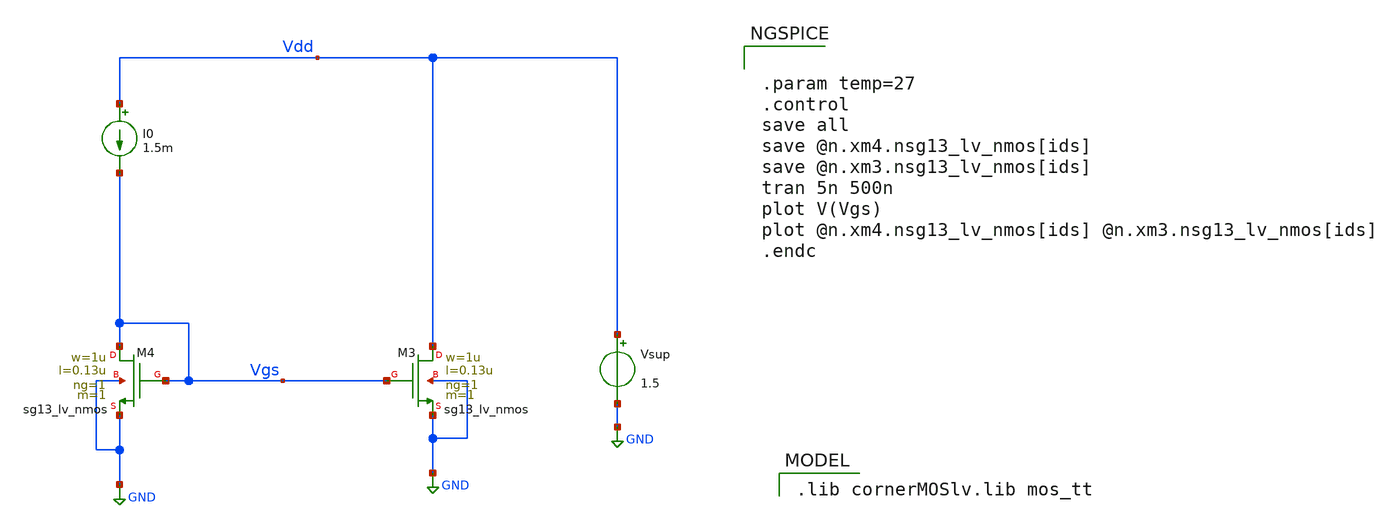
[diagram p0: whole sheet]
** sch_path: xschem/current_mirror.sch
**.subckt current_mirror
XM3 Vdd Vgs GND GND sg13_lv_nmos w=1u l=0.13u ng=1 m=1 mm_ok=1
XM4 Vgs Vgs GND GND sg13_lv_nmos w=1u l=0.13u ng=1 m=1 mm_ok=1
Vsup Vdd GND 1.5
I0 Vdd Vgs 1.5m
**** begin user architecture code
 .lib cornerMOSlv.lib mos_tt



.param temp=27
.control
save all
save @n.xm4.nsg13_lv_nmos[ids]
save @n.xm3.nsg13_lv_nmos[ids]
tran 5n 500n
plot V(Vgs)
plot @n.xm4.nsg13_lv_nmos[ids] @n.xm3.nsg13_lv_nmos[ids]
.endc


**** end user architecture code
**.ends
.GLOBAL GND
.end
